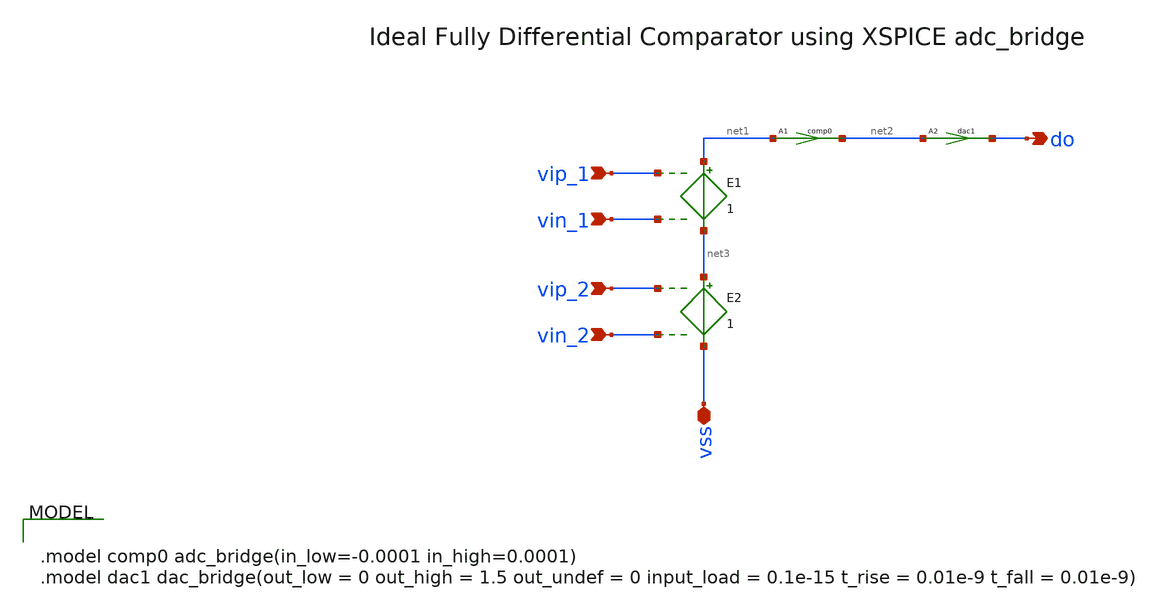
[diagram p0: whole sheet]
** sch_path: xschem/comp-macro.sch
**.subckt comp-macro vss vip_1 vin_1 vip_2 vin_2 do
*.iopin vss
*.ipin vip_1
*.ipin vin_1
*.ipin vip_2
*.ipin vin_2
*.opin do
A1 [ net1 ] [ net2 ] comp0
E1 net1 net3 vip_1 vin_1 1
E2 net3 vss vip_2 vin_2 1
A2 [ net2 ] [ do ] dac1
**.ends
**** begin user architecture code


.model comp0 adc_bridge(in_low=-0.0001 in_high=0.0001)
.model dac1 dac_bridge(out_low = 0 out_high = 1.5 out_undef = 0 input_load = 0.1e-15 t_rise =
+ 0.01e-9 t_fall = 0.01e-9)


**** end user architecture code
.end
